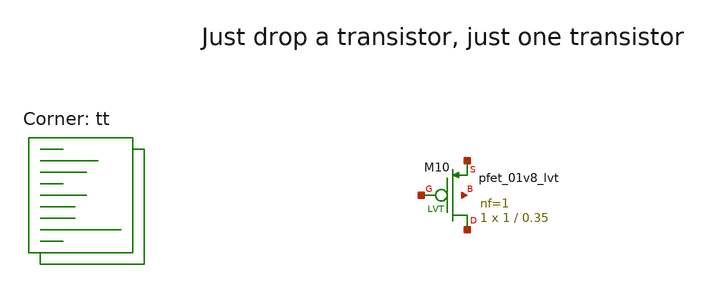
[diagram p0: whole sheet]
** sch_path: automatization_analog_design/mos_dc_characteristic/mos.sch
**.subckt mos
XM10 net1 net2 net3 net4 sky130_fd_pr__pfet_01v8_lvt L=0.35 W=1 nf=1 ad='int((1 + 1)/2) * 1 / 1 * 0.29'
+ as='int((1 + 2)/2) * 1 / 1 * 0.29' pd='2*int((1 + 1)/2) * (1 / 1 + 0.29)' ps='2*int((1 + 2)/2) * (1 / 1 + 0.29)'
+ nrd='0.29 / 1 ' nrs='0.29 / 1 ' sa=0 sb=0 sd=0 mult=1 m=1
**** begin user architecture code

**************************************************************
**************************************************************
**************************************************************
**************************************************************
**************************************************************
*LIBs*********************************************************
**************************************************************
**************************************************************
**************************************************************
**************************************************************
**************************************************************
*.lib $::SKYWATER_MODELS/sky130.lib.spice tt
* chose the corners in the corner file
* tt_mm for mismatch
* ss ff sf fs standart corners
* ll hh lh hl capacitor and resistors corners
* mc for total process variation including corners
**************************************************************
**************************************************************
**************************************************************
**************************************************************
**************************************************************
*Corners/montecarlo options***********************************
**************************************************************
**************************************************************
**************************************************************
**************************************************************
**************************************************************
.TEMP 27
**************************************************************
**************************************************************
**************************************************************
**************************************************************
*SIMULATION and Plots*****************************************
**************************************************************
**************************************************************
**************************************************************
**************************************************************
.control
save all
.endc

.lib $::SKYWATER_MODELS/sky130.lib.spice tt
**** end user architecture code
**.ends
.end
